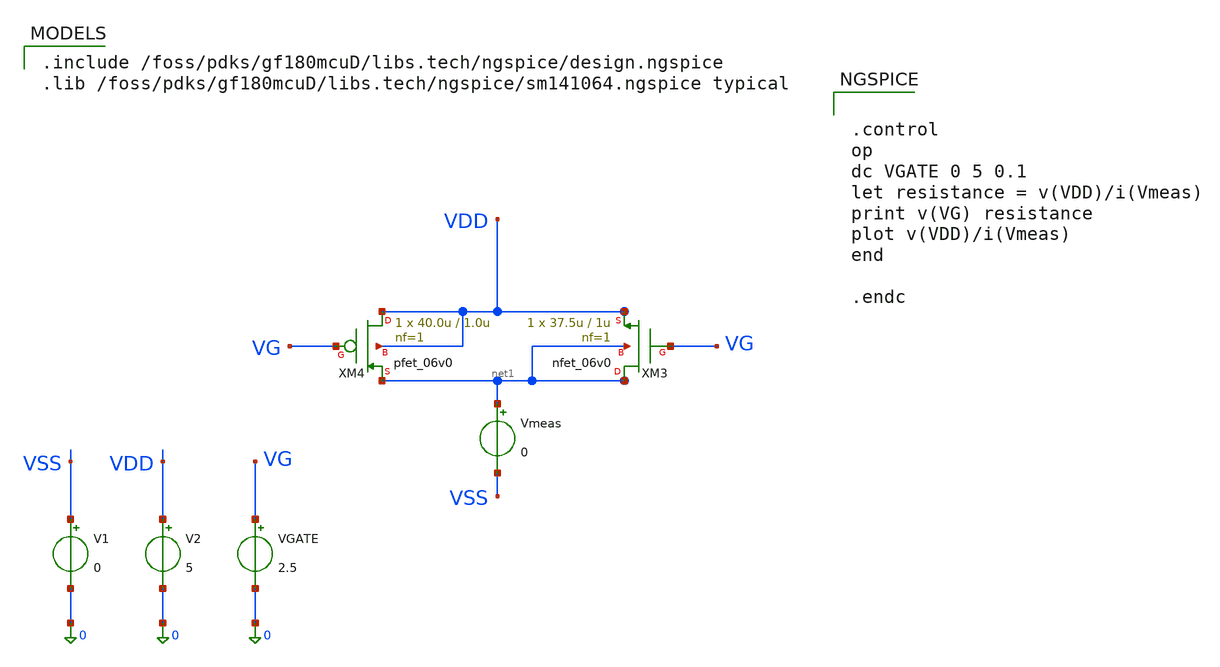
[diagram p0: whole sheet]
** sch_path: activities/opamp3An/N_PMOS1kresistor.sch
**.subckt N_PMOS1kresistor
XM3 net1 VG VDD net1 nfet_06v0 L=1u W=37.5u nf=1 ad='int((nf+1)/2) * W/nf * 0.18u' as='int((nf+2)/2) * W/nf * 0.18u'
+ pd='2*int((nf+1)/2) * (W/nf + 0.18u)' ps='2*int((nf+2)/2) * (W/nf + 0.18u)' nrd='0.18u / W' nrs='0.18u / W'
+ sa=0 sb=0 sd=0 m=1
XM4 VDD VG net1 VDD pfet_06v0 L=1.0u W=40.0u nf=1 ad='int((nf+1)/2) * W/nf * 0.18u' as='int((nf+2)/2) * W/nf * 0.18u'
+ pd='2*int((nf+1)/2) * (W/nf + 0.18u)' ps='2*int((nf+2)/2) * (W/nf + 0.18u)' nrd='0.18u / W' nrs='0.18u / W'
+ sa=0 sb=0 sd=0 m=1
V1 VSS 0 0
V2 VDD 0 5
VGATE VG 0 2.5
Vmeas net1 VSS 0
**** begin user architecture code


.control
op
dc VGATE 0 5 0.1
let resistance = v(VDD)/i(Vmeas)
print v(VG) resistance
plot v(VDD)/i(Vmeas)
end

.endc


.include /foss/pdks/gf180mcuD/libs.tech/ngspice/design.ngspice
.lib /foss/pdks/gf180mcuD/libs.tech/ngspice/sm141064.ngspice typical

**** end user architecture code
**.ends
.end
